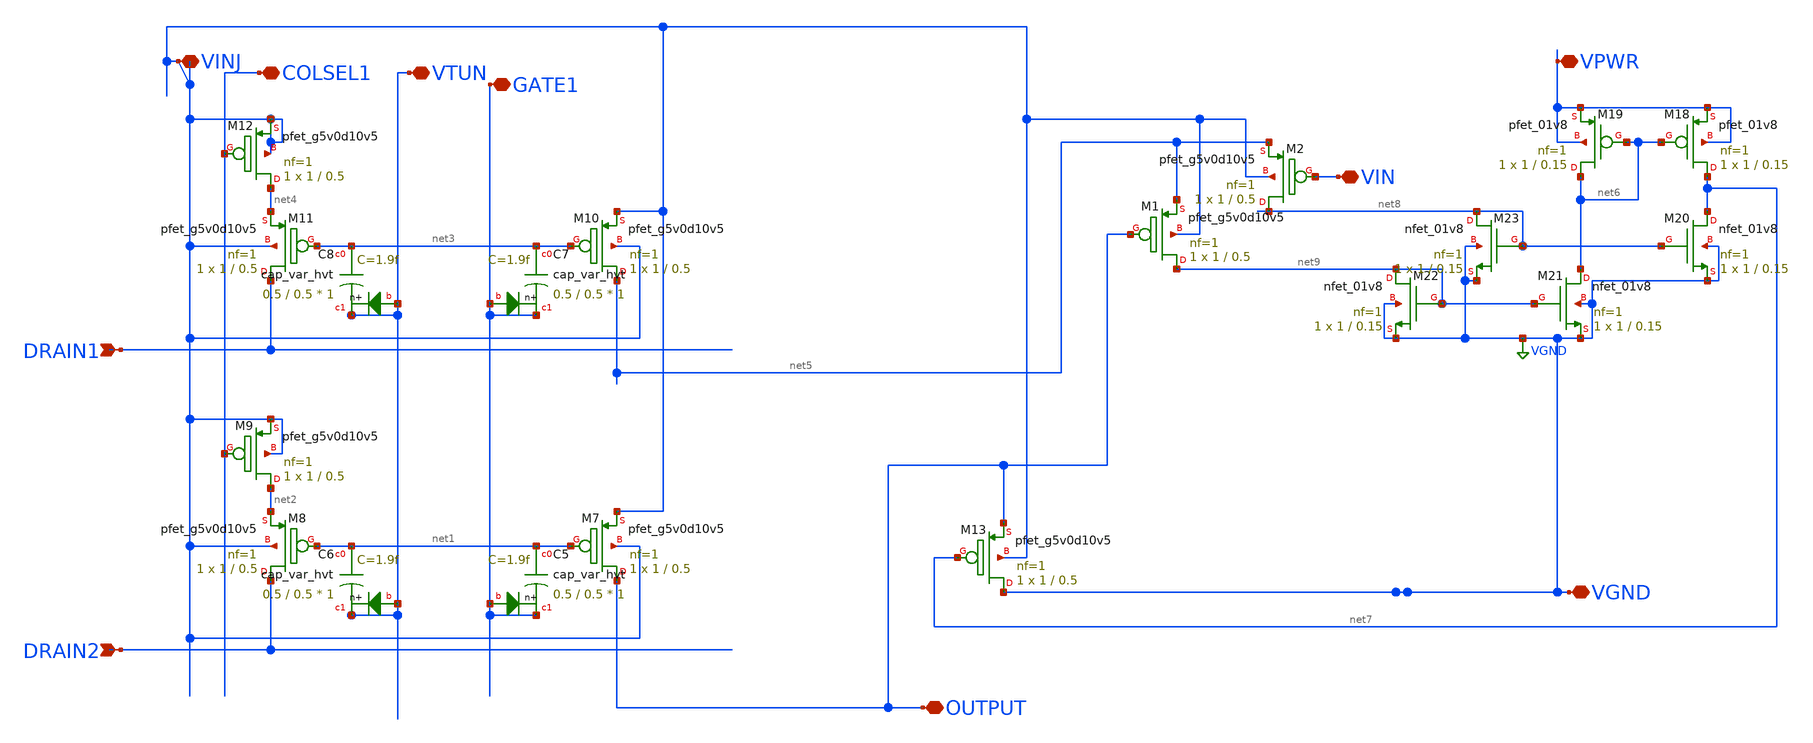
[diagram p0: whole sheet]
** sch_path: libs.ref/sky130_hilas_sc/xschem/sky130_hilas_AmpDetect01.sch
**.subckt sky130_hilas_AmpDetect01 DRAIN1 DRAIN2 VPWR GATE1 VTUN COLSEL1 VINJ OUTPUT VIN VGND
*.ipin DRAIN1
*.ipin DRAIN2
*.iopin VPWR
*.iopin GATE1
*.iopin VTUN
*.iopin COLSEL1
*.iopin VINJ
*.iopin OUTPUT
*.iopin VIN
*.iopin VGND
XM7 OUTPUT net1 VINJ VINJ sky130_fd_pr__pfet_g5v0d10v5 L=0.5 W=1 nf=1 ad='int((nf+1)/2) * W/nf * 0.29'
+ as='int((nf+2)/2) * W/nf * 0.29' pd='2*int((nf+1)/2) * (W/nf + 0.29)' ps='2*int((nf+2)/2) * (W/nf + 0.29)'
+ nrd='0.29 / W' nrs='0.29 / W' sa=0 sb=0 sd=0 mult=1 m=1
XC5 net1 GATE1 GATE1 sky130_fd_pr__cap_var_hvt W=0.5 L=0.5 VM=1 m=1
XM8 DRAIN2 net1 net2 VINJ sky130_fd_pr__pfet_g5v0d10v5 L=0.5 W=1 nf=1 ad='int((nf+1)/2) * W/nf * 0.29'
+ as='int((nf+2)/2) * W/nf * 0.29' pd='2*int((nf+1)/2) * (W/nf + 0.29)' ps='2*int((nf+2)/2) * (W/nf + 0.29)'
+ nrd='0.29 / W' nrs='0.29 / W' sa=0 sb=0 sd=0 mult=1 m=1
XC6 net1 VTUN VTUN sky130_fd_pr__cap_var_hvt W=0.5 L=0.5 VM=1 m=1
XM9 net2 COLSEL1 VINJ VINJ sky130_fd_pr__pfet_g5v0d10v5 L=0.5 W=1 nf=1 ad='int((nf+1)/2) * W/nf * 0.29'
+ as='int((nf+2)/2) * W/nf * 0.29' pd='2*int((nf+1)/2) * (W/nf + 0.29)' ps='2*int((nf+2)/2) * (W/nf + 0.29)'
+ nrd='0.29 / W' nrs='0.29 / W' sa=0 sb=0 sd=0 mult=1 m=1
XM10 net5 net3 VINJ VINJ sky130_fd_pr__pfet_g5v0d10v5 L=0.5 W=1 nf=1 ad='int((nf+1)/2) * W/nf * 0.29'
+ as='int((nf+2)/2) * W/nf * 0.29' pd='2*int((nf+1)/2) * (W/nf + 0.29)' ps='2*int((nf+2)/2) * (W/nf + 0.29)'
+ nrd='0.29 / W' nrs='0.29 / W' sa=0 sb=0 sd=0 mult=1 m=1
XC7 net3 GATE1 GATE1 sky130_fd_pr__cap_var_hvt W=0.5 L=0.5 VM=1 m=1
XM11 DRAIN1 net3 net4 VINJ sky130_fd_pr__pfet_g5v0d10v5 L=0.5 W=1 nf=1 ad='int((nf+1)/2) * W/nf * 0.29'
+ as='int((nf+2)/2) * W/nf * 0.29' pd='2*int((nf+1)/2) * (W/nf + 0.29)' ps='2*int((nf+2)/2) * (W/nf + 0.29)'
+ nrd='0.29 / W' nrs='0.29 / W' sa=0 sb=0 sd=0 mult=1 m=1
XC8 net3 VTUN VTUN sky130_fd_pr__cap_var_hvt W=0.5 L=0.5 VM=1 m=1
XM12 net4 COLSEL1 VINJ VINJ sky130_fd_pr__pfet_g5v0d10v5 L=0.5 W=1 nf=1 ad='int((nf+1)/2) * W/nf * 0.29'
+ as='int((nf+2)/2) * W/nf * 0.29' pd='2*int((nf+1)/2) * (W/nf + 0.29)' ps='2*int((nf+2)/2) * (W/nf + 0.29)'
+ nrd='0.29 / W' nrs='0.29 / W' sa=0 sb=0 sd=0 mult=1 m=1
XM18 net7 net6 VPWR VPWR sky130_fd_pr__pfet_01v8 L=0.15 W=1 nf=1 ad='int((nf+1)/2) * W/nf * 0.29' as='int((nf+2)/2) * W/nf * 0.29'
+ pd='2*int((nf+1)/2) * (W/nf + 0.29)' ps='2*int((nf+2)/2) * (W/nf + 0.29)' nrd='0.29 / W' nrs='0.29 / W'
+ sa=0 sb=0 sd=0 mult=1 m=1
XM19 net6 net6 VPWR VPWR sky130_fd_pr__pfet_01v8 L=0.15 W=1 nf=1 ad='int((nf+1)/2) * W/nf * 0.29' as='int((nf+2)/2) * W/nf * 0.29'
+ pd='2*int((nf+1)/2) * (W/nf + 0.29)' ps='2*int((nf+2)/2) * (W/nf + 0.29)' nrd='0.29 / W' nrs='0.29 / W'
+ sa=0 sb=0 sd=0 mult=1 m=1
XM20 net7 net8 VGND VGND sky130_fd_pr__nfet_01v8 L=0.15 W=1 nf=1 ad='int((nf+1)/2) * W/nf * 0.29' as='int((nf+2)/2) * W/nf * 0.29'
+ pd='2*int((nf+1)/2) * (W/nf + 0.29)' ps='2*int((nf+2)/2) * (W/nf + 0.29)' nrd='0.29 / W' nrs='0.29 / W'
+ sa=0 sb=0 sd=0 mult=1 m=1
XM21 net6 net9 VGND VGND sky130_fd_pr__nfet_01v8 L=0.15 W=1 nf=1 ad='int((nf+1)/2) * W/nf * 0.29' as='int((nf+2)/2) * W/nf * 0.29'
+ pd='2*int((nf+1)/2) * (W/nf + 0.29)' ps='2*int((nf+2)/2) * (W/nf + 0.29)' nrd='0.29 / W' nrs='0.29 / W'
+ sa=0 sb=0 sd=0 mult=1 m=1
XM22 net9 net9 VGND VGND sky130_fd_pr__nfet_01v8 L=0.15 W=1 nf=1 ad='int((nf+1)/2) * W/nf * 0.29' as='int((nf+2)/2) * W/nf * 0.29'
+ pd='2*int((nf+1)/2) * (W/nf + 0.29)' ps='2*int((nf+2)/2) * (W/nf + 0.29)' nrd='0.29 / W' nrs='0.29 / W'
+ sa=0 sb=0 sd=0 mult=1 m=1
XM23 net8 net8 VGND VGND sky130_fd_pr__nfet_01v8 L=0.15 W=1 nf=1 ad='int((nf+1)/2) * W/nf * 0.29' as='int((nf+2)/2) * W/nf * 0.29'
+ pd='2*int((nf+1)/2) * (W/nf + 0.29)' ps='2*int((nf+2)/2) * (W/nf + 0.29)' nrd='0.29 / W' nrs='0.29 / W'
+ sa=0 sb=0 sd=0 mult=1 m=1
XM13 VGND net7 OUTPUT VINJ sky130_fd_pr__pfet_g5v0d10v5 L=0.5 W=1 nf=1 ad='int((nf+1)/2) * W/nf * 0.29'
+ as='int((nf+2)/2) * W/nf * 0.29' pd='2*int((nf+1)/2) * (W/nf + 0.29)' ps='2*int((nf+2)/2) * (W/nf + 0.29)'
+ nrd='0.29 / W' nrs='0.29 / W' sa=0 sb=0 sd=0 mult=1 m=1
XM1 net9 OUTPUT net5 VINJ sky130_fd_pr__pfet_g5v0d10v5 L=0.5 W=1 nf=1 ad='int((nf+1)/2) * W/nf * 0.29'
+ as='int((nf+2)/2) * W/nf * 0.29' pd='2*int((nf+1)/2) * (W/nf + 0.29)' ps='2*int((nf+2)/2) * (W/nf + 0.29)'
+ nrd='0.29 / W' nrs='0.29 / W' sa=0 sb=0 sd=0 mult=1 m=1
XM2 net8 VIN net5 VINJ sky130_fd_pr__pfet_g5v0d10v5 L=0.5 W=1 nf=1 ad='int((nf+1)/2) * W/nf * 0.29' as='int((nf+2)/2) * W/nf * 0.29'
+ pd='2*int((nf+1)/2) * (W/nf + 0.29)' ps='2*int((nf+2)/2) * (W/nf + 0.29)' nrd='0.29 / W' nrs='0.29 / W'
+ sa=0 sb=0 sd=0 mult=1 m=1
**.ends
.GLOBAL VGND
.end
